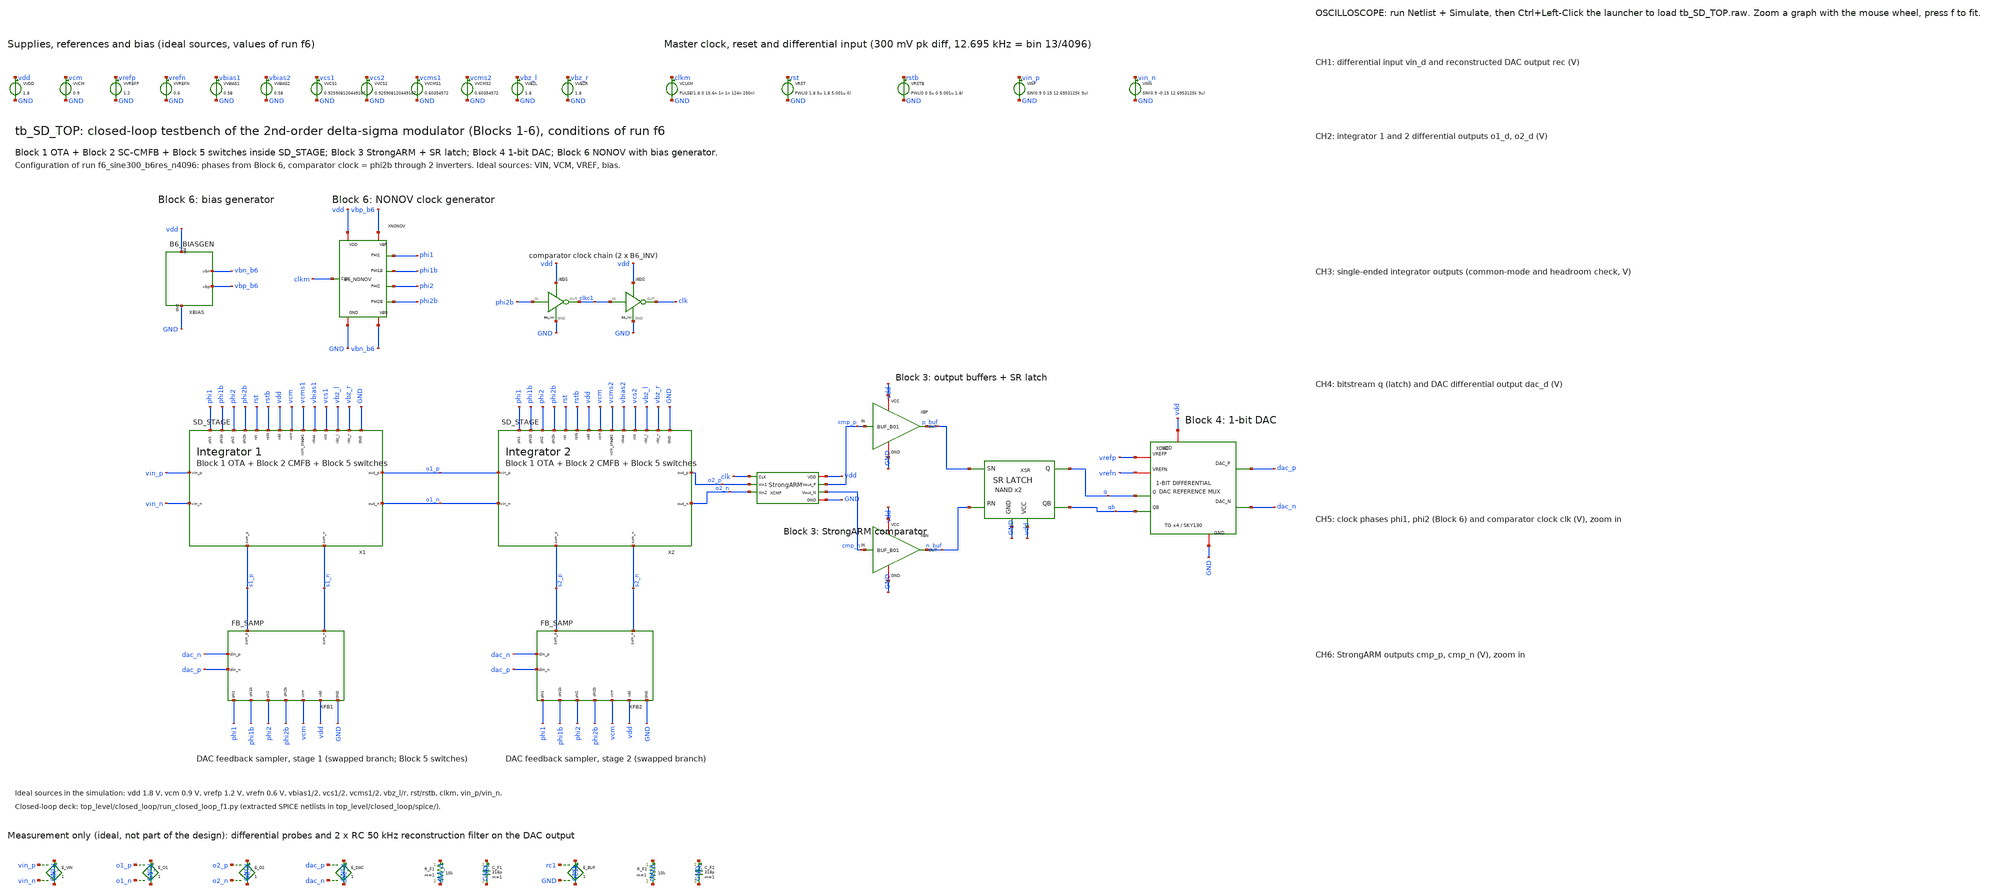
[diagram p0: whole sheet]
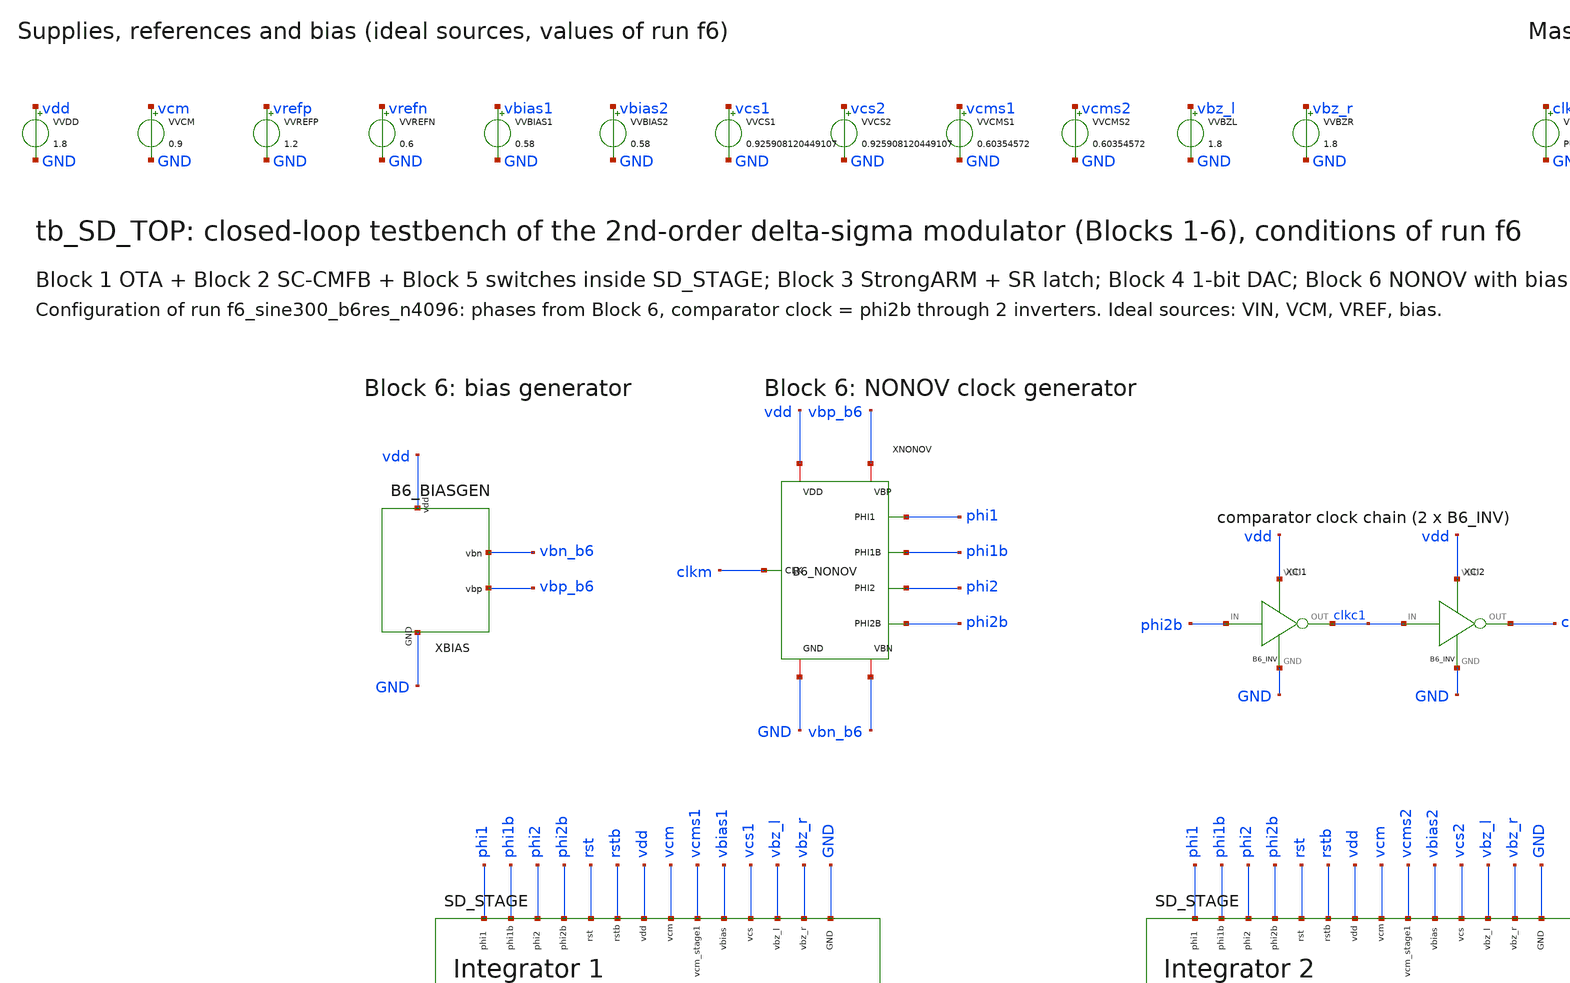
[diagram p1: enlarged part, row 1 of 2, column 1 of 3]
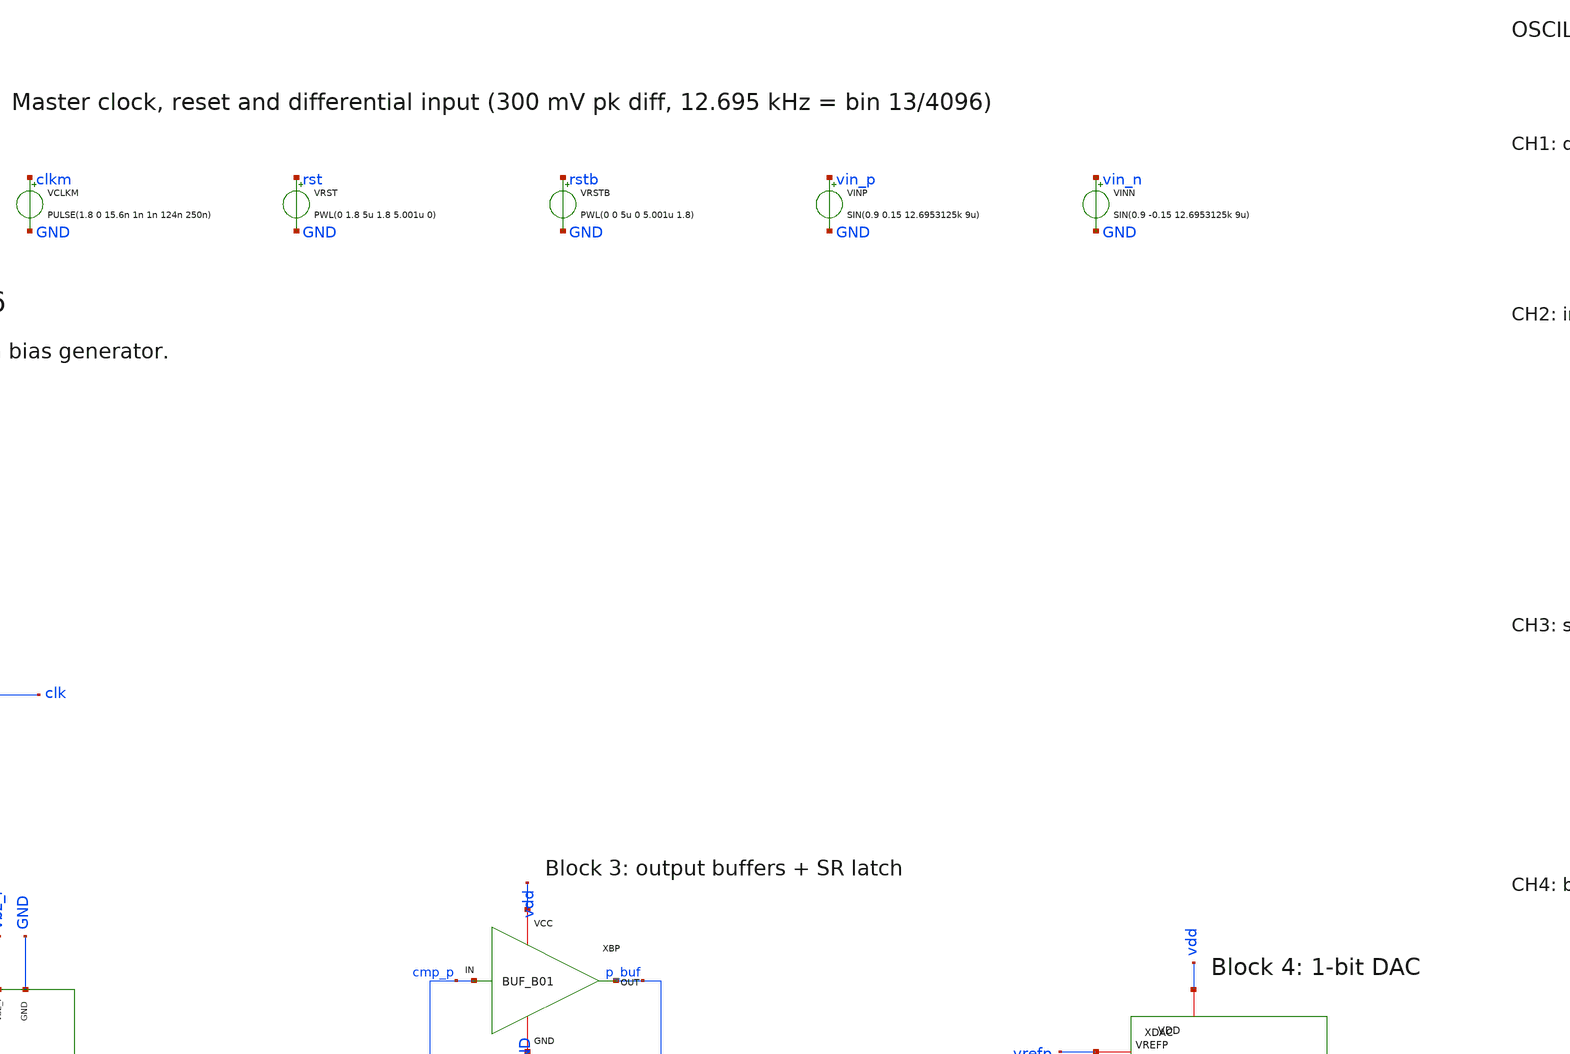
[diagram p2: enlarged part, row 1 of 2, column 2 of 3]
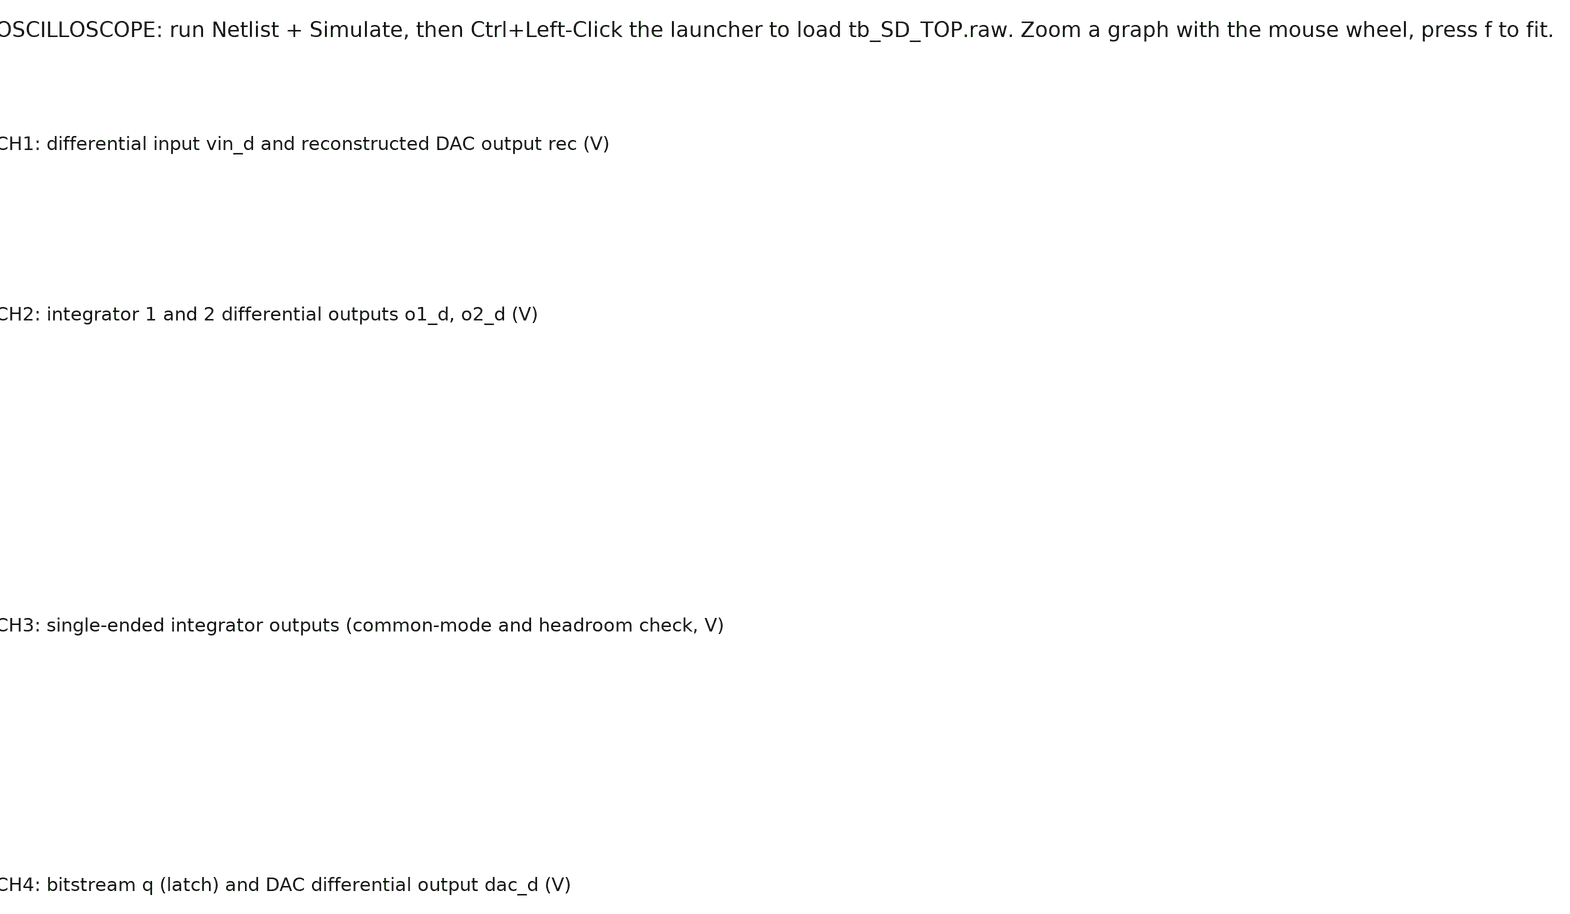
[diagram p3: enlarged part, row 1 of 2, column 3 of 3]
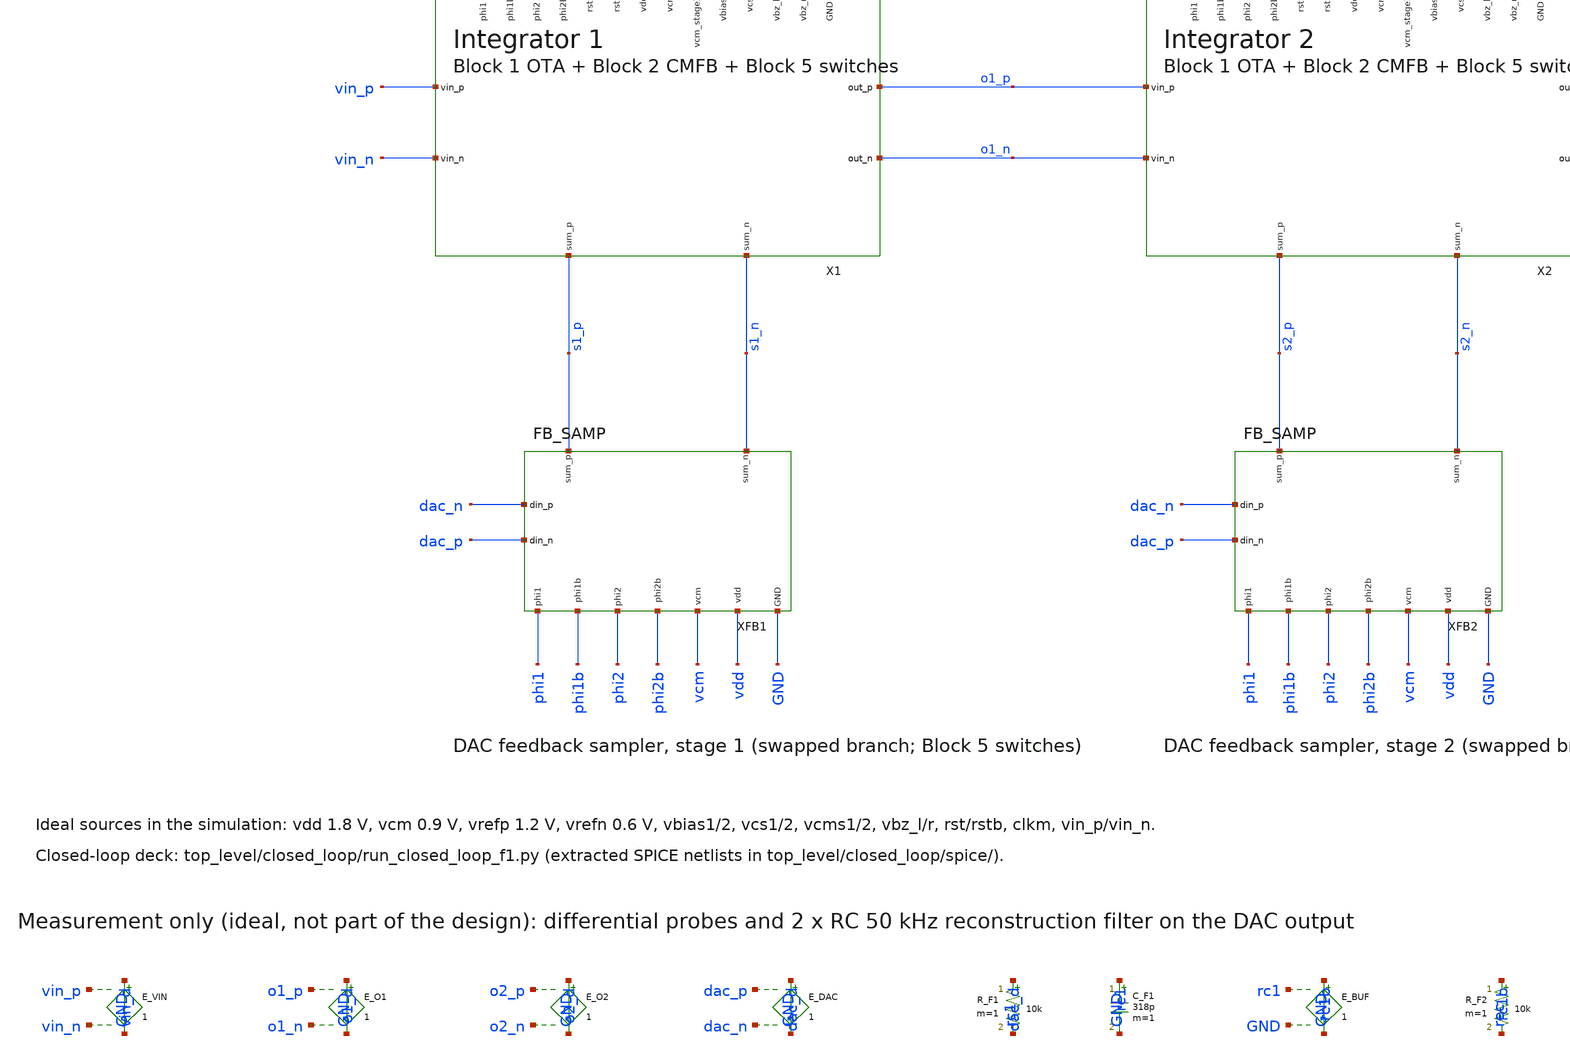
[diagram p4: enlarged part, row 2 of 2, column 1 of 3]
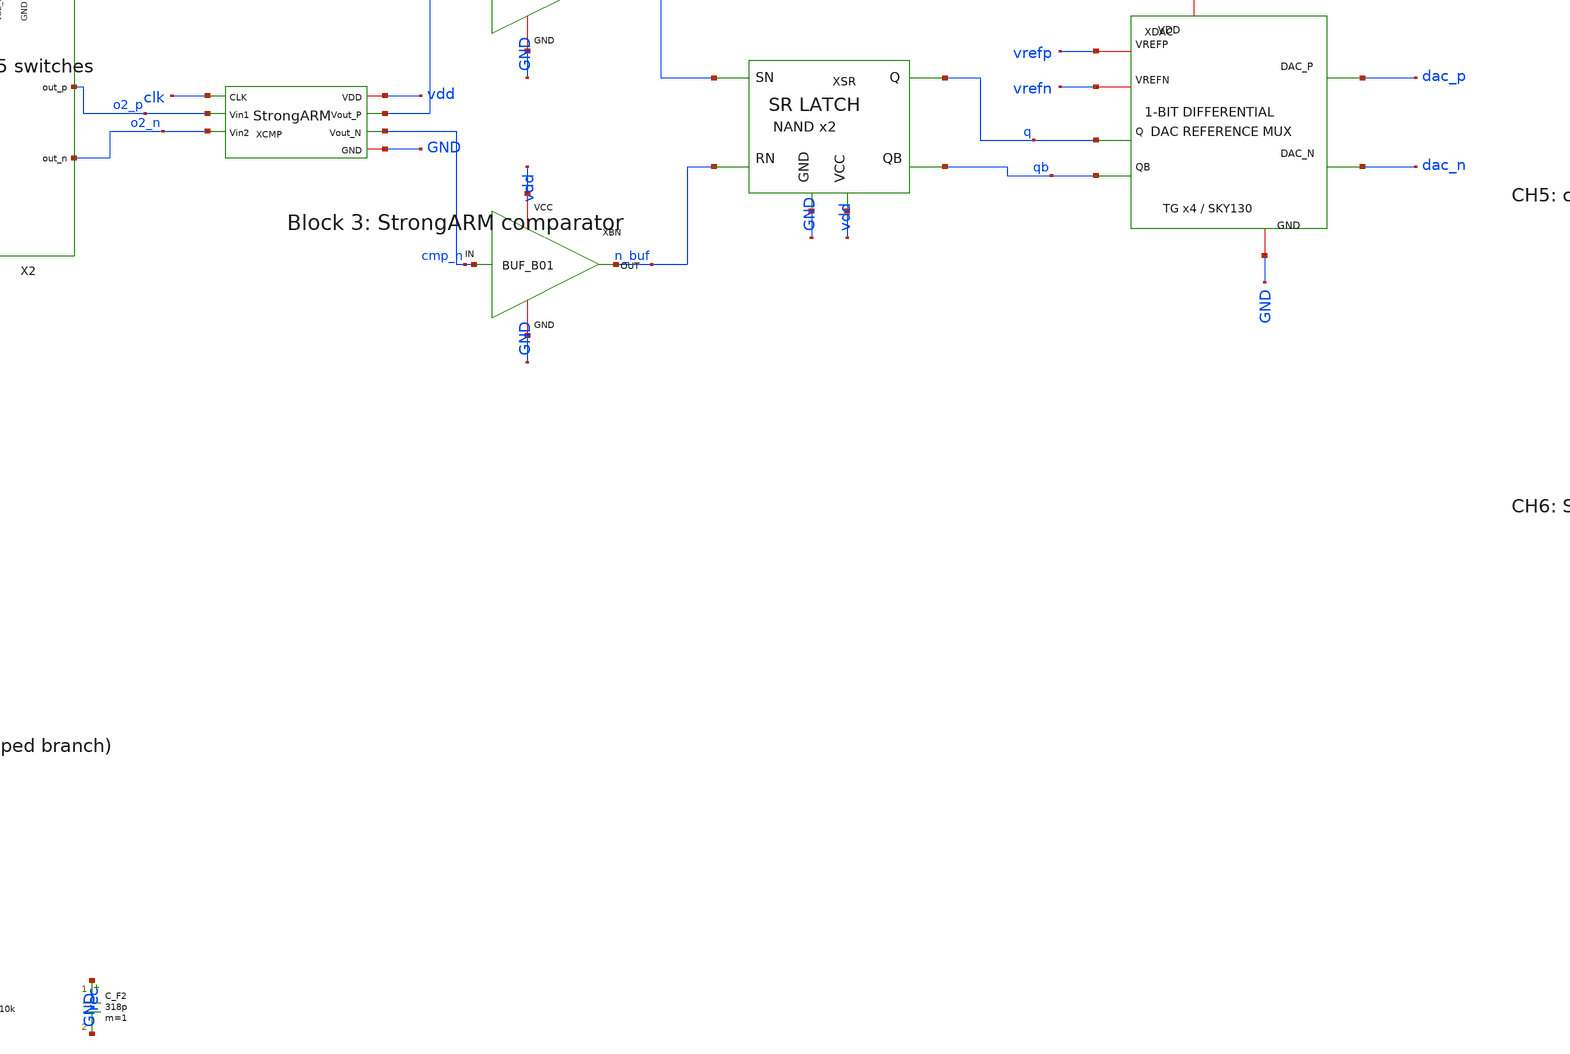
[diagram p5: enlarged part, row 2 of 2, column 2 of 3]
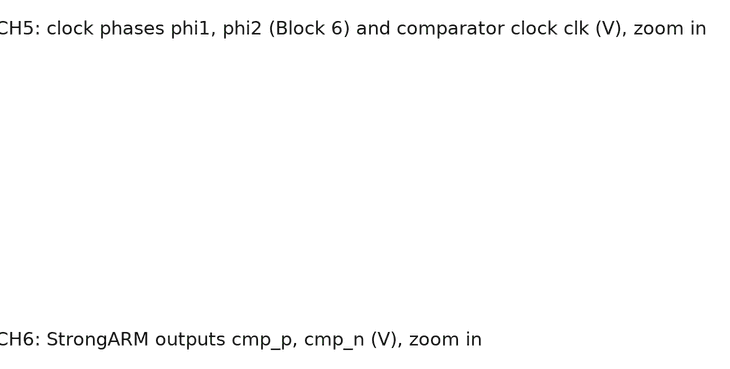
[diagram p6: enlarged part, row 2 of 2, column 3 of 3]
** sch_path: top_level/xschem/tb_SD_TOP.sch
**.subckt tb_SD_TOP
X1 vin_p vin_n o1_p o1_n s1_p s1_n phi1 phi1b phi2 phi2b rst rstb vdd vcm vcms1 vbias1 vcs1 vbz_l
+ vbz_r GND SD_STAGE
X2 o1_p o1_n o2_p o2_n s2_p s2_n phi1 phi1b phi2 phi2b rst rstb vdd vcm vcms2 vbias2 vcs2 vbz_l
+ vbz_r GND SD_STAGE
XCMP vdd clk cmp_p cmp_n o2_p o2_n GND StrongARM
XBP vdd cmp_p p_buf GND BUF_B01
XBN vdd cmp_n n_buf GND BUF_B01
XSR p_buf n_buf q qb GND vdd SR_Latch
XDAC vrefp vrefn q qb vdd GND dac_p dac_n DAC_1bit
XFB1 dac_n dac_p s1_p s1_n phi1 phi1b phi2 phi2b vcm vdd GND FB_SAMP
XFB2 dac_n dac_p s2_p s2_n phi1 phi1b phi2 phi2b vcm vdd GND FB_SAMP
XNONOV clkm phi1 phi1b phi2 phi2b vdd vbp_b6 GND vbn_b6 B6_NONOV
XBIAS vdd GND vbn_b6 vbp_b6 B6_BIASGEN
XCI1 phi2b clkc1 vdd GND B6_INV
XCI2 clkc1 clk vdd GND B6_INV
VVDD vdd GND 1.8
VVCM vcm GND 0.9
VVREFP vrefp GND 1.2
VVREFN vrefn GND 0.6
VVBIAS1 vbias1 GND 0.58
VVBIAS2 vbias2 GND 0.58
VVCS1 vcs1 GND 0.925908120449107
VVCS2 vcs2 GND 0.925908120449107
VVCMS1 vcms1 GND 0.60354572
VVCMS2 vcms2 GND 0.60354572
VVBZL vbz_l GND 1.8
VVBZR vbz_r GND 1.8
VCLKM clkm GND PULSE(1.8 0 15.6n 1n 1n 124n 250n)
VRST rst GND PWL(0 1.8 5u 1.8 5.001u 0)
VRSTB rstb GND PWL(0 0 5u 0 5.001u 1.8)
VINP vin_p GND SIN(0.9 0.15 12.6953125k 9u)
VINN vin_n GND SIN(0.9 -0.15 12.6953125k 9u)
E_VIN vin_d GND vin_p vin_n 1
E_O1 o1_d GND o1_p o1_n 1
E_O2 o2_d GND o2_p o2_n 1
E_DAC dac_d GND dac_p dac_n 1
R_F1 dac_d rc1 10k m=1
C_F1 rc1 GND 318p m=1
E_BUF rc1b GND rc1 GND 1
R_F2 rc1b rec 10k m=1
C_F2 rec GND 318p m=1
**** begin user architecture code


.lib /foss/pdks/sky130A/libs.tech/combined/sky130.lib.spice tt
.option scale=1e-6
.option reltol=1e-5 vntol=1e-8 abstol=1e-13
.temp 27
.nodeset v(q)=0 v(qb)=1.8

* Quick look: 90 us = 5 us reset + about one input period (78.8 us).
* Full SNDR run (1.03325 ms, 4096 bits) stays in top_level/closed_loop/run_closed_loop_f1.py.
.control
save v(vin_p) v(vin_n) v(vin_d) v(rec) v(dac_p) v(dac_n) v(dac_d)
save v(o1_p) v(o1_n) v(o1_d) v(o2_p) v(o2_n) v(o2_d) v(s1_p) v(s1_n) v(s2_p) v(s2_n)
save v(cmp_p) v(cmp_n) v(p_buf) v(n_buf) v(q) v(qb)
save v(clkm) v(phi1) v(phi1b) v(phi2) v(phi2b) v(clk) v(rst) v(vbn_b6) v(vbp_b6)
tran 1n 90u 0 100p
linearize
write tb_SD_TOP.raw
.endc


**** end user architecture code
**.ends
.end
